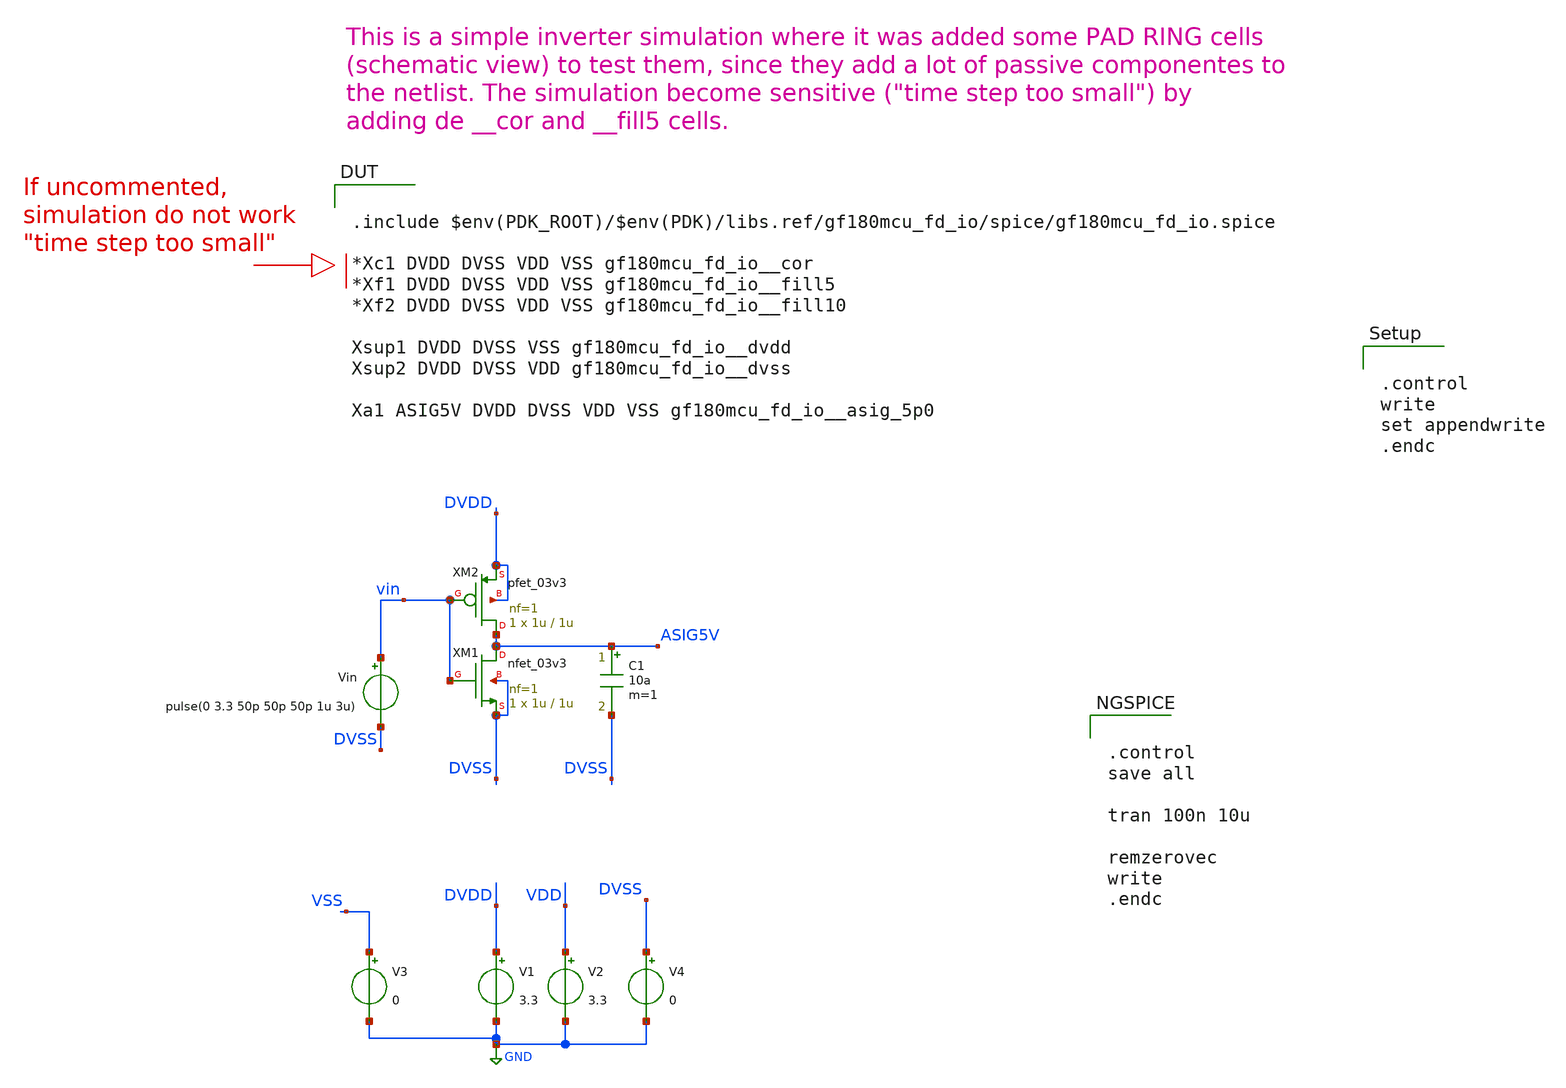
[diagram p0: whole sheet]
** sch_path: padframe/concatenation_switching_asig_5p0/test/concatenation_switching_asig_5p0.sch

.control
write
set appendwrite
.endc
**.subckt concatenation_switching_asig_5p0
V1 DVDD GND 3.3
V2 VDD GND 3.3
Vin vin DVSS pulse(0 3.3 50p 50p 50p 1u 3u)
C1 ASIG5V DVSS 10a m=1
V3 VSS GND 0
V4 DVSS GND 0
XM1 ASIG5V vin DVSS DVSS nfet_03v3 L=1u W=1u nf=1 ad='int((nf+1)/2) * W/nf * 0.18u' as='int((nf+2)/2) * W/nf * 0.18u'
+ pd='2*int((nf+1)/2) * (W/nf + 0.18u)' ps='2*int((nf+2)/2) * (W/nf + 0.18u)' nrd='0.18u / W' nrs='0.18u / W'
+ sa=0 sb=0 sd=0 m=1
XM2 ASIG5V vin DVDD DVDD pfet_03v3 L=1u W=1u nf=1 ad='int((nf+1)/2) * W/nf * 0.18u' as='int((nf+2)/2) * W/nf * 0.18u'
+ pd='2*int((nf+1)/2) * (W/nf + 0.18u)' ps='2*int((nf+2)/2) * (W/nf + 0.18u)' nrd='0.18u / W' nrs='0.18u / W'
+ sa=0 sb=0 sd=0 m=1
**** begin user architecture code

.include $env(PDK_ROOT)/$env(PDK)/libs.tech/ngspice/design.ngspice
.lib $env(PDK_ROOT)/$env(PDK)/libs.tech/ngspice/sm141064.ngspice typical
.lib $env(PDK_ROOT)/$env(PDK)/libs.tech/ngspice/sm141064.ngspice diode_typical
.lib $env(PDK_ROOT)/$env(PDK)/libs.tech/ngspice/sm141064.ngspice res_typical
.lib $env(PDK_ROOT)/$env(PDK)/libs.tech/ngspice/sm141064.ngspice mimcap_typical
.lib $env(PDK_ROOT)/$env(PDK)/libs.tech/ngspice/sm141064.ngspice moscap_typical


.include $env(PDK_ROOT)/$env(PDK)/libs.ref/gf180mcu_fd_io/spice/gf180mcu_fd_io.spice

*Xc1 DVDD DVSS VDD VSS gf180mcu_fd_io__cor
*Xf1 DVDD DVSS VDD VSS gf180mcu_fd_io__fill5
*Xf2 DVDD DVSS VDD VSS gf180mcu_fd_io__fill10

Xsup1 DVDD DVSS VSS gf180mcu_fd_io__dvdd
Xsup2 DVDD DVSS VDD gf180mcu_fd_io__dvss

Xa1 ASIG5V DVDD DVSS VDD VSS gf180mcu_fd_io__asig_5p0




.control
save all

tran 100n 10u

remzerovec
write
.endc

**** end user architecture code
**.ends
.GLOBAL GND
.end
